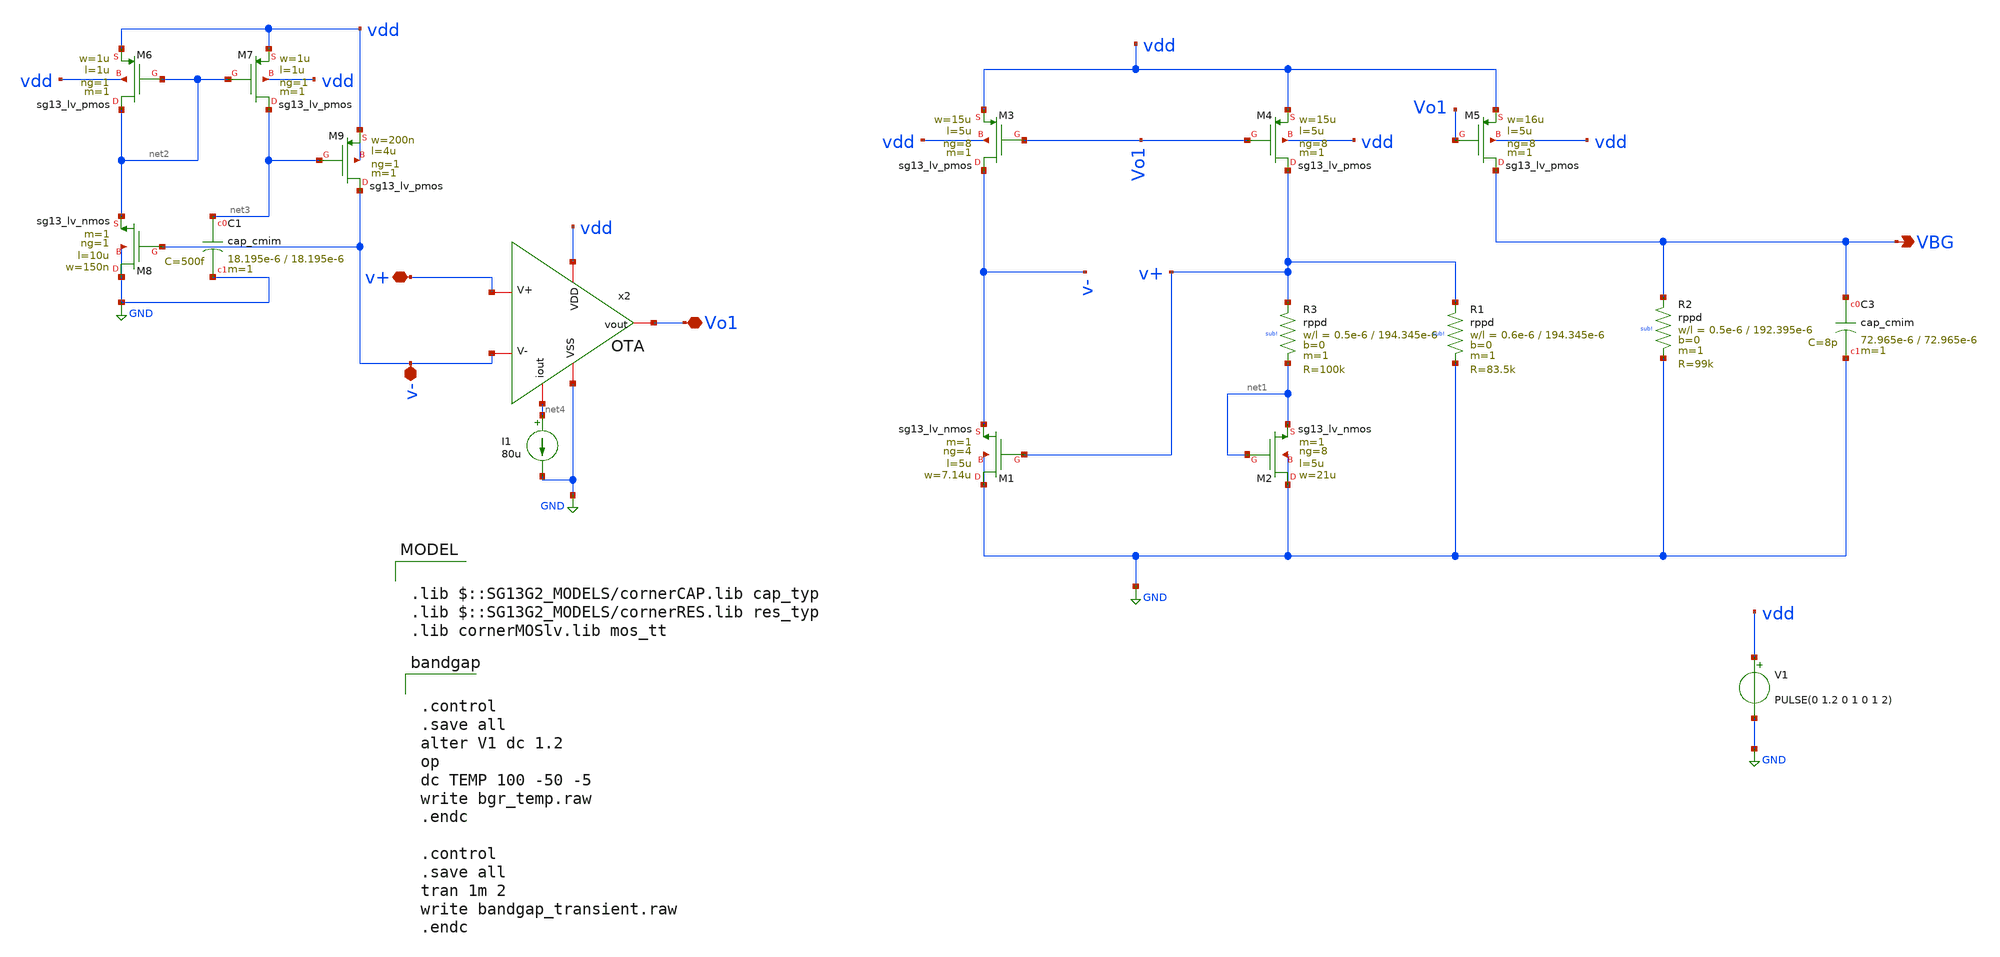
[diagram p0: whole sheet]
** sch_path: BTDay7-Ex/bandgap_reference.sch
**.subckt bandgap_reference VBG v+ v- Vo1
*.opin VBG
*.iopin v+
*.iopin v-
*.iopin Vo1
V1 vdd GND PULSE(0 1.2 0 1 0 1 2)
XM1 GND v+ v- GND sg13_lv_nmos w=7.14u l=5u ng=4 m=1 mm_ok=1
XM2 GND net1 net1 GND sg13_lv_nmos w=21u l=5u ng=8 m=1 mm_ok=1
XM3 v- Vo1 vdd vdd sg13_lv_pmos w=15u l=5u ng=8 m=1 mm_ok=1
XM4 v+ Vo1 vdd vdd sg13_lv_pmos w=15u l=5u ng=8 m=1 mm_ok=1
XM5 VBG Vo1 vdd vdd sg13_lv_pmos w=16u l=5u ng=8 m=1 mm_ok=1
XC3 VBG GND cap_cmim w=72.965e-6 l=72.965e-6 m=1 mm_ok=1
XR3 v+ net1 sub! rppd w=0.5e-6 l=194.345e-6 m=1 b=0 mm_ok=1
XR1 v+ GND sub! rppd w=0.6e-6 l=194.345e-6 m=1 b=0 mm_ok=1
XR2 VBG GND sub! rppd w=0.5e-6 l=192.395e-6 m=1 b=0 mm_ok=1
XM8 GND v- net2 GND sg13_lv_nmos w=150n l=10u ng=1 m=1 mm_ok=1
XM6 net2 net2 vdd vdd sg13_lv_pmos w=1u l=1u ng=1 m=1 mm_ok=1
XM7 net3 net2 vdd vdd sg13_lv_pmos w=1u l=1u ng=1 m=1 mm_ok=1
XM9 v- net3 vdd vdd sg13_lv_pmos w=200n l=4u ng=1 m=1 mm_ok=1
I1 net4 GND 80u
XC1 net3 GND cap_cmim w=18.195e-6 l=18.195e-6 m=1 mm_ok=1
x2 v- v+ GND vdd net4 Vo1 OTA
**** begin user architecture code


.control
.save all
alter V1 dc 1.2
op
dc TEMP 100 -50 -5
write bgr_temp.raw
.endc

.control
.save all
tran 1m 2
write bandgap_transient.raw
.endc



.lib $::SG13G2_MODELS/cornerCAP.lib cap_typ
.lib $::SG13G2_MODELS/cornerRES.lib res_typ
.lib cornerMOSlv.lib mos_tt

**** end user architecture code
**.ends

* expanding   symbol:  /foss/designs/BTDay7-Ex/OTA.sym # of pins=6
** sym_path: BTDay7-Ex/OTA.sym
** sch_path: BTDay7-Ex/OTA.sch
.subckt OTA V- V+ VSS VDD iout vout
*.iopin VDD
*.iopin iout
*.iopin V-
*.iopin VSS
*.iopin V+
*.iopin vout
XM6 iout iout VDD VDD sg13_lv_pmos w=75u l=2.08u ng=8 m=1 mm_ok=1
XM7 net1 iout VDD VDD sg13_lv_pmos w=5.3u l=1.95u ng=1 m=1 mm_ok=1
XM8 net3 V- net1 VDD sg13_lv_pmos w=7.41u l=3.64u ng=1 m=1 mm_ok=1
XM9 net2 V+ net1 VDD sg13_lv_pmos w=7.41u l=3.64u ng=1 m=1 mm_ok=1
XM10 net3 net3 VSS VSS sg13_lv_nmos w=720n l=9.75u ng=1 m=1 mm_ok=1
XM11 net2 net3 VSS VSS sg13_lv_nmos w=720n l=9.75u ng=1 m=1 mm_ok=1
XM1 vout net2 VSS VSS sg13_lv_nmos w=28.8u l=9.75u ng=4 m=1 mm_ok=1
XM2 vout iout VDD VDD sg13_lv_pmos w=75u l=2.08u ng=8 m=1 mm_ok=1
XC1 net2 vout cap_cmim w=22.295e-6 l=22.295e-6 m=1 mm_ok=1
.ends

.GLOBAL GND
.end
